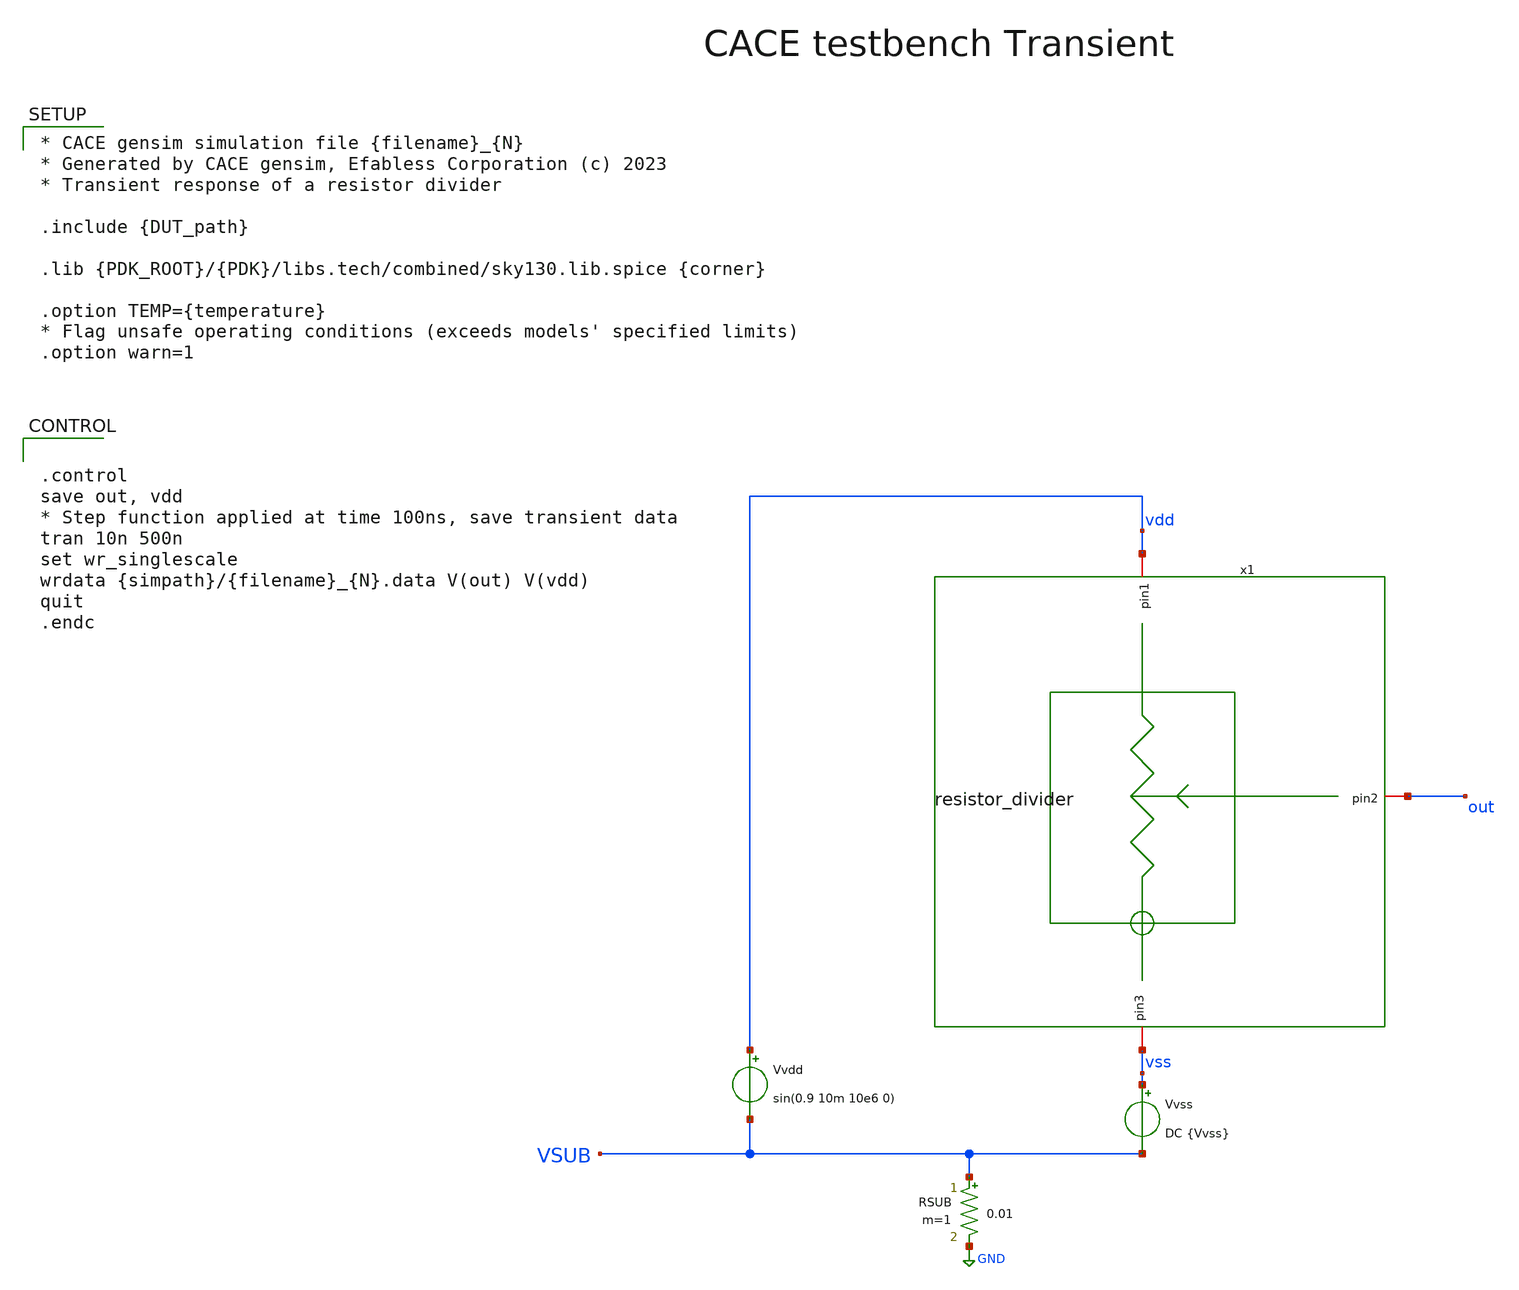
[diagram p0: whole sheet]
** sch_path: resistor_divider/cace/transient.sch
**.subckt transient
Vvdd vdd VSUB sin(0.9 10m 10e6 0)
Vvss vss VSUB DC {Vvss}
RSUB VSUB GND 0.01 m=1
x1 vdd out vss resistor_divider
**** begin user architecture code


.control
save out, vdd
* Step function applied at time 100ns, save transient data
tran 10n 500n
set wr_singlescale
wrdata {simpath}/{filename}_{N}.data V(out) V(vdd)
quit
.endc



* CACE gensim simulation file {filename}_{N}
* Generated by CACE gensim, Efabless Corporation (c) 2023
* Transient response of a resistor divider

.include {DUT_path}

.lib {PDK_ROOT}/{PDK}/libs.tech/combined/sky130.lib.spice {corner}

.option TEMP={temperature}
* Flag unsafe operating conditions (exceeds models' specified limits)
.option warn=1


**** end user architecture code
**.ends

* expanding   symbol:  ../xschem/resistor_divider.sym # of pins=3
** sym_path: resistor_divider/xschem/resistor_divider.sym
** sch_path: resistor_divider/xschem/resistor_divider.sch
.subckt resistor_divider pin1 pin2 pin3
*.iopin pin1
*.iopin pin3
*.iopin pin2
XR1 pin2 pin1 pin3 sky130_fd_pr__res_high_po_0p35 L=3.5 mult=1 m=1
XR2 pin3 pin2 pin3 sky130_fd_pr__res_high_po_0p35 L=3.5 mult=1 m=1
.ends

.GLOBAL GND
.end
